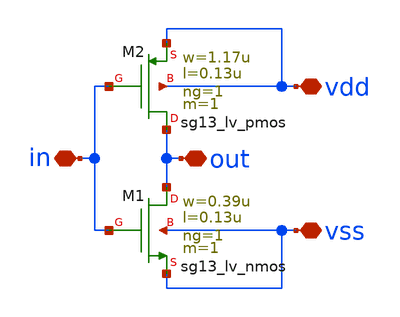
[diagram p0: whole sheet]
** sch_path: design/blocks/inverter/schematic/inverter.sch
**.subckt inverter vdd out vss in
*.iopin vdd
*.iopin out
*.iopin vss
*.iopin in
XM1 out in vss vss sg13_lv_nmos w=0.39u l=0.13u ng=1 m=1 mm_ok=1
XM2 out in vdd vdd sg13_lv_pmos w=1.17u l=0.13u ng=1 m=1 mm_ok=1
**.ends
.end
